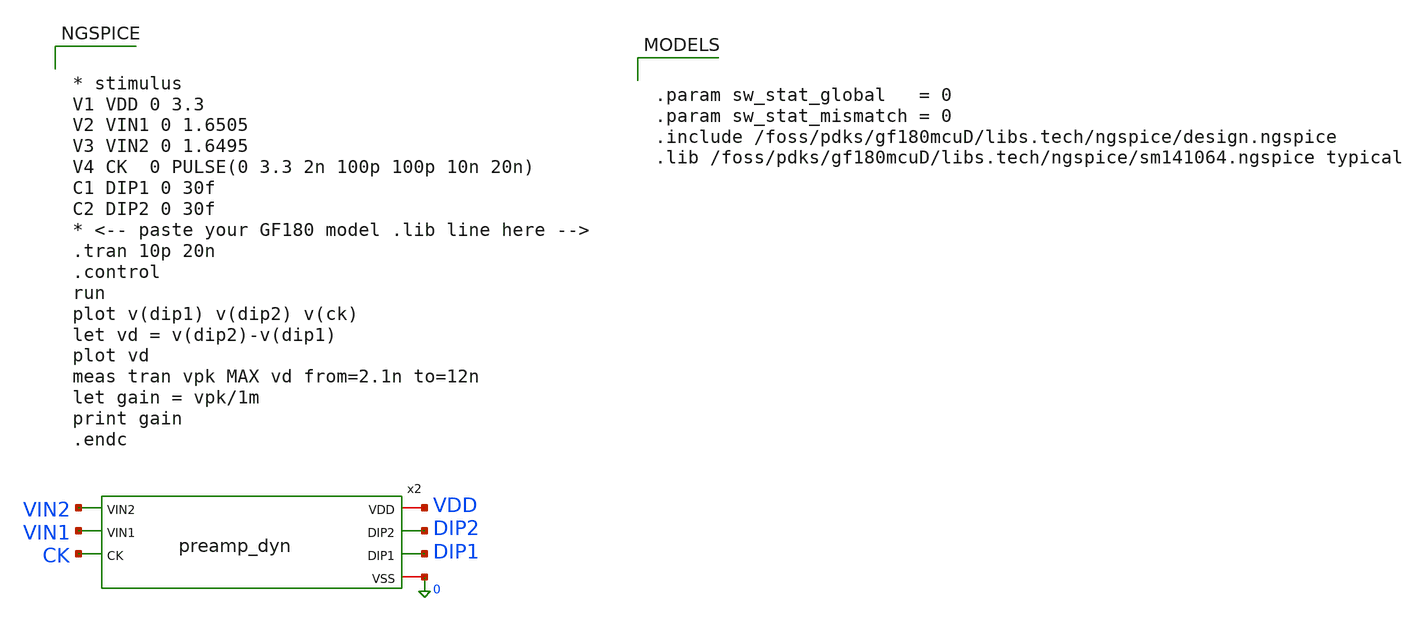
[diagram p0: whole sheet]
** sch_path: comparator_alt/schematic/tb_preamp.sch
**.subckt tb_preamp
x2 VDD DIP2 DIP1 VIN2 VIN1 CK 0 preamp_dyn
**** begin user architecture code


* stimulus
V1 VDD 0 3.3
V2 VIN1 0 1.6505
V3 VIN2 0 1.6495
V4 CK  0 PULSE(0 3.3 2n 100p 100p 10n 20n)
C1 DIP1 0 30f
C2 DIP2 0 30f
* <-- paste your GF180 model .lib line here -->
.tran 10p 20n
.control
run
plot v(dip1) v(dip2) v(ck)
let vd = v(dip2)-v(dip1)
plot vd
meas tran vpk MAX vd from=2.1n to=12n
let gain = vpk/1m
print gain
.endc




.param sw_stat_global   = 0
.param sw_stat_mismatch = 0
.include /foss/pdks/gf180mcuD/libs.tech/ngspice/design.ngspice
.lib /foss/pdks/gf180mcuD/libs.tech/ngspice/sm141064.ngspice typical


**** end user architecture code
**.ends

* expanding   symbol:  comparator_alt/schematic/preamp_dyn.sym # of pins=7
** sym_path: comparator_alt/schematic/preamp_dyn.sym
** sch_path: comparator_alt/schematic/preamp_dyn.sch
.subckt preamp_dyn VDD DIP2 DIP1 VIN2 VIN1 CK VSS
*.ipin VIN1
*.ipin VIN2
*.iopin VDD
*.iopin VSS
*.opin DIP1
*.opin DIP2
*.ipin CK
XM1P DIP1 VIN1 TAIL VSS nfet_03v3 L=1u W=4u nf=1 ad='int((nf+1)/2) * W/nf * 0.18u' as='int((nf+2)/2) * W/nf * 0.18u'
+ pd='2*int((nf+1)/2) * (W/nf + 0.18u)' ps='2*int((nf+2)/2) * (W/nf + 0.18u)' nrd='0.18u / W' nrs='0.18u / W'
+ sa=0 sb=0 sd=0 m=16
XMT1 TAIL CK VSS VSS nfet_03v3 L=1u W=1u nf=1 ad='int((nf+1)/2) * W/nf * 0.18u' as='int((nf+2)/2) * W/nf * 0.18u'
+ pd='2*int((nf+1)/2) * (W/nf + 0.18u)' ps='2*int((nf+2)/2) * (W/nf + 0.18u)' nrd='0.18u / W' nrs='0.18u / W'
+ sa=0 sb=0 sd=0 m=1
XM2P DIP2 VIN2 TAIL VSS nfet_03v3 L=1u W=4u nf=1 ad='int((nf+1)/2) * W/nf * 0.18u' as='int((nf+2)/2) * W/nf * 0.18u'
+ pd='2*int((nf+1)/2) * (W/nf + 0.18u)' ps='2*int((nf+2)/2) * (W/nf + 0.18u)' nrd='0.18u / W' nrs='0.18u / W'
+ sa=0 sb=0 sd=0 m=16
XMP1 DIP1 CK VDD VDD pfet_03v3 L=0.3u W=3u nf=1 ad='int((nf+1)/2) * W/nf * 0.18u' as='int((nf+2)/2) * W/nf * 0.18u'
+ pd='2*int((nf+1)/2) * (W/nf + 0.18u)' ps='2*int((nf+2)/2) * (W/nf + 0.18u)' nrd='0.18u / W' nrs='0.18u / W'
+ sa=0 sb=0 sd=0 m=1
XMP2 DIP2 CK VDD VDD pfet_03v3 L=0.3u W=3u nf=1 ad='int((nf+1)/2) * W/nf * 0.18u' as='int((nf+2)/2) * W/nf * 0.18u'
+ pd='2*int((nf+1)/2) * (W/nf + 0.18u)' ps='2*int((nf+2)/2) * (W/nf + 0.18u)' nrd='0.18u / W' nrs='0.18u / W'
+ sa=0 sb=0 sd=0 m=1
.ends

.end
